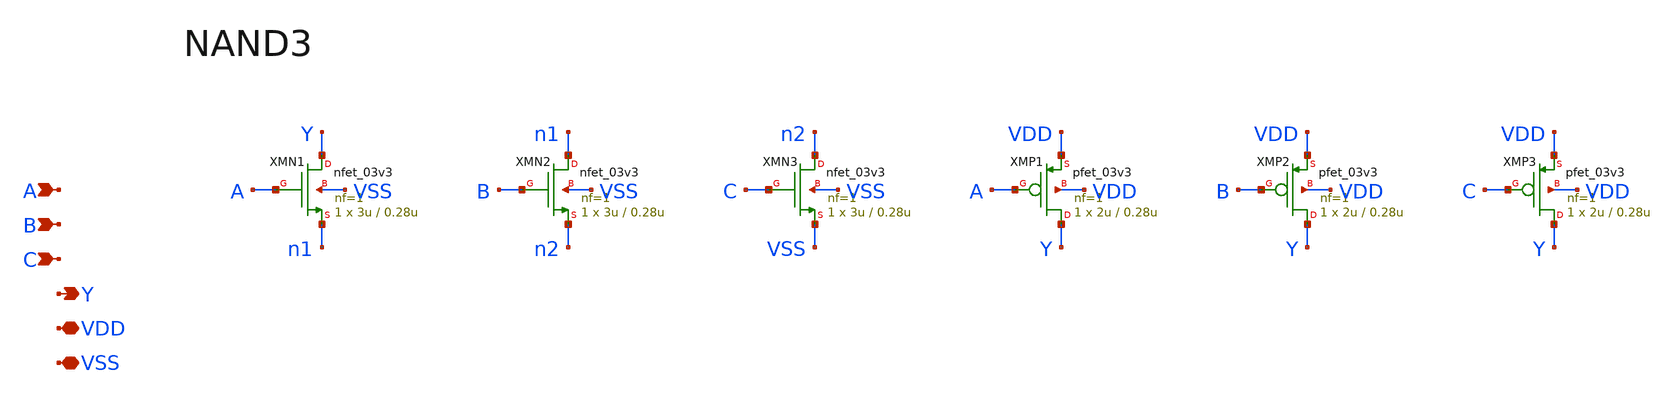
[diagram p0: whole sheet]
** sch_path: v1_claude/xschem/nand3.sch
**.subckt nand3 A B C Y VDD VSS
*.ipin A
*.ipin B
*.ipin C
*.opin Y
*.iopin VDD
*.iopin VSS
XMN1 Y A n1 VSS nfet_03v3 L=0.28u W=3u nf=1 ad='int((nf+1)/2) * W/nf * 0.18u' as='int((nf+2)/2) * W/nf * 0.18u'
+ pd='2*int((nf+1)/2) * (W/nf + 0.18u)' ps='2*int((nf+2)/2) * (W/nf + 0.18u)' nrd='0.18u / W' nrs='0.18u / W'
+ sa=0 sb=0 sd=0 m=1
XMN2 n1 B n2 VSS nfet_03v3 L=0.28u W=3u nf=1 ad='int((nf+1)/2) * W/nf * 0.18u' as='int((nf+2)/2) * W/nf * 0.18u'
+ pd='2*int((nf+1)/2) * (W/nf + 0.18u)' ps='2*int((nf+2)/2) * (W/nf + 0.18u)' nrd='0.18u / W' nrs='0.18u / W'
+ sa=0 sb=0 sd=0 m=1
XMN3 n2 C VSS VSS nfet_03v3 L=0.28u W=3u nf=1 ad='int((nf+1)/2) * W/nf * 0.18u' as='int((nf+2)/2) * W/nf * 0.18u'
+ pd='2*int((nf+1)/2) * (W/nf + 0.18u)' ps='2*int((nf+2)/2) * (W/nf + 0.18u)' nrd='0.18u / W' nrs='0.18u / W'
+ sa=0 sb=0 sd=0 m=1
XMP1 Y A VDD VDD pfet_03v3 L=0.28u W=2u nf=1 ad='int((nf+1)/2) * W/nf * 0.18u' as='int((nf+2)/2) * W/nf * 0.18u'
+ pd='2*int((nf+1)/2) * (W/nf + 0.18u)' ps='2*int((nf+2)/2) * (W/nf + 0.18u)' nrd='0.18u / W' nrs='0.18u / W'
+ sa=0 sb=0 sd=0 m=1
XMP2 Y B VDD VDD pfet_03v3 L=0.28u W=2u nf=1 ad='int((nf+1)/2) * W/nf * 0.18u' as='int((nf+2)/2) * W/nf * 0.18u'
+ pd='2*int((nf+1)/2) * (W/nf + 0.18u)' ps='2*int((nf+2)/2) * (W/nf + 0.18u)' nrd='0.18u / W' nrs='0.18u / W'
+ sa=0 sb=0 sd=0 m=1
XMP3 Y C VDD VDD pfet_03v3 L=0.28u W=2u nf=1 ad='int((nf+1)/2) * W/nf * 0.18u' as='int((nf+2)/2) * W/nf * 0.18u'
+ pd='2*int((nf+1)/2) * (W/nf + 0.18u)' ps='2*int((nf+2)/2) * (W/nf + 0.18u)' nrd='0.18u / W' nrs='0.18u / W'
+ sa=0 sb=0 sd=0 m=1
**.ends
.end
